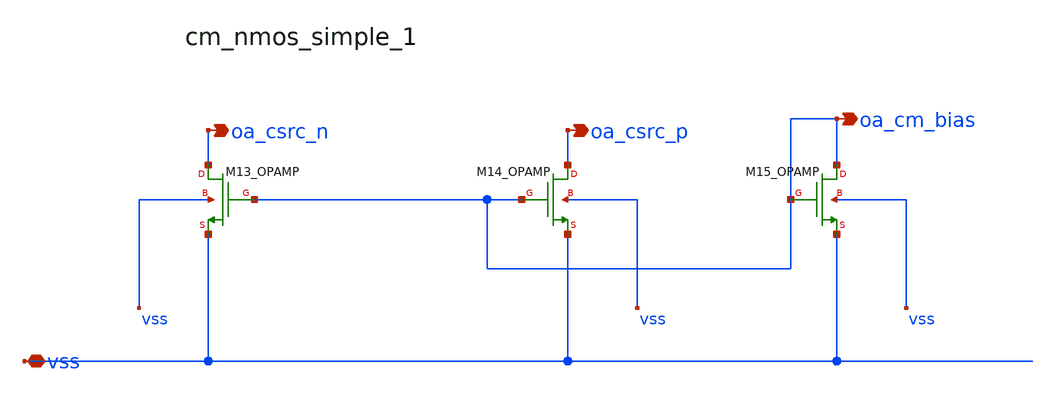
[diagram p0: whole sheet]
** sch_path: analog-db/raw/sup_003_rrl_sc_integrator/hier/blocks/cm_nmos_simple_1.sch
**.subckt cm_nmos_simple_1 vss oa_csrc_n oa_csrc_p oa_cm_bias
*.iopin vss
*.opin oa_csrc_n
*.opin oa_csrc_p
*.opin oa_cm_bias
XM13_OPAMP oa_csrc_n oa_cm_bias vss vss sg13_lv_nmos w=x_dut_xm13_opamp_w l=x_dut_xm13_opamp_l ng=1
+ m=x_dut_xm13_opamp_m
XM14_OPAMP oa_csrc_p oa_cm_bias vss vss sg13_lv_nmos w=x_dut_xm14_opamp_w l=x_dut_xm14_opamp_l ng=1
+ m=x_dut_xm14_opamp_m
XM15_OPAMP oa_cm_bias oa_cm_bias vss vss sg13_lv_nmos w=x_dut_xm15_opamp_w l=x_dut_xm15_opamp_l ng=1
+ m=x_dut_xm15_opamp_m
**.ends
.end
